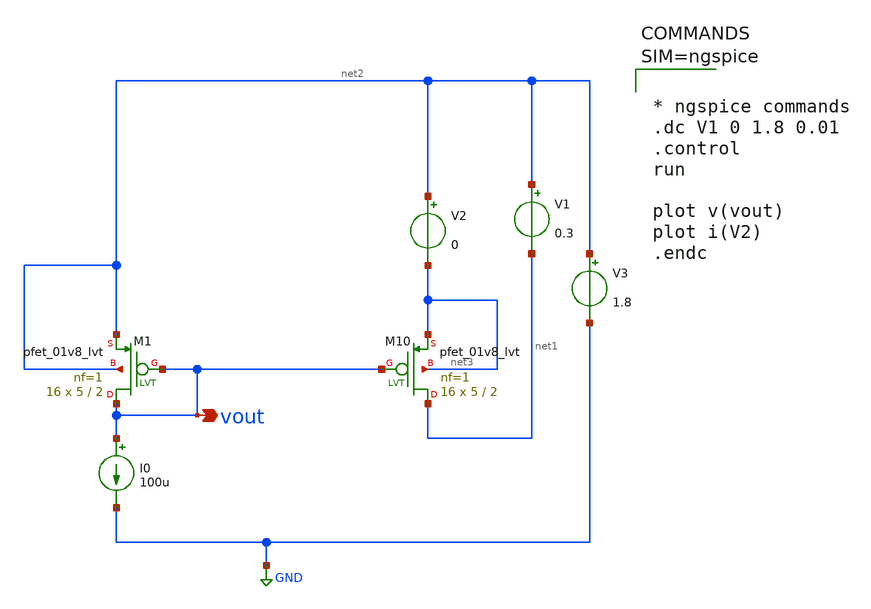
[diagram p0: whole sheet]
** sch_path: xschem/pmos_out_imp.sch
**.subckt pmos_out_imp vout
*.opin vout
XM10 net1 vout net3 net3 sky130_fd_pr__pfet_01v8_lvt L=2 W=5 nf=1 ad='int((1 + 1)/2) * 5 / 1 * 0.29'
+ as='int((1 + 2)/2) * 5 / 1 * 0.29' pd='2*int((1 + 1)/2) * (5 / 1 + 0.29)' ps='2*int((1 + 2)/2) * (5 / 1 + 0.29)'
+ nrd='0.29 / 5 ' nrs='0.29 / 5 ' sa=0 sb=0 sd=0 mult=16 m=16
XM1 vout vout net2 net2 sky130_fd_pr__pfet_01v8_lvt L=2 W=5 nf=1 ad='int((1 + 1)/2) * 5 / 1 * 0.29' as='int((1 + 2)/2) * 5 / 1 * 0.29'
+ pd='2*int((1 + 1)/2) * (5 / 1 + 0.29)' ps='2*int((1 + 2)/2) * (5 / 1 + 0.29)' nrd='0.29 / 5 ' nrs='0.29 / 5 '
+ sa=0 sb=0 sd=0 mult=16 m=16
I0 vout GND 100u
V2 net2 net3 0
V3 net2 GND 1.8
V1 net2 net1 0.3
**** begin user architecture code

** opencircuitdesign pdks install
.lib $::SKYWATER_MODELS/sky130.lib.spice tt




* ngspice commands
.dc V1 0 1.8 0.01
.control
run

plot v(vout)
plot i(V2)
.endc



**** end user architecture code
**.ends
.GLOBAL GND
.end
